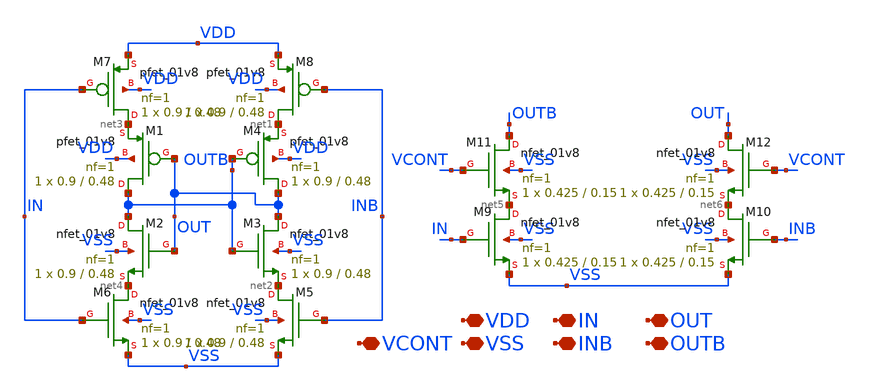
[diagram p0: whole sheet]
** sch_path: xschem/xschem_BGR_Top/Sigma_Delta/VCO/VCO_Delay.sch
**.subckt VCO_Delay VDD VSS IN INB OUT OUTB VCONT
*.iopin VDD
*.iopin VSS
*.iopin IN
*.iopin INB
*.iopin OUT
*.iopin OUTB
*.iopin VCONT
XM4 OUT OUTB net1 VDD sky130_fd_pr__pfet_01v8 L=0.48 W=0.9 nf=1 ad='int((nf+1)/2) * W/nf * 0.29' as='int((nf+2)/2) * W/nf * 0.29'
+ pd='2*int((nf+1)/2) * (W/nf + 0.29)' ps='2*int((nf+2)/2) * (W/nf + 0.29)' nrd='0.29 / W' nrs='0.29 / W'
+ sa=0 sb=0 sd=0 mult=1 m=1
XM3 OUT OUTB net2 VSS sky130_fd_pr__nfet_01v8 L=0.48 W=0.9 nf=1 ad='int((nf+1)/2) * W/nf * 0.29' as='int((nf+2)/2) * W/nf * 0.29'
+ pd='2*int((nf+1)/2) * (W/nf + 0.29)' ps='2*int((nf+2)/2) * (W/nf + 0.29)' nrd='0.29 / W' nrs='0.29 / W'
+ sa=0 sb=0 sd=0 mult=1 m=1
XM1 OUTB OUT net3 VDD sky130_fd_pr__pfet_01v8 L=0.48 W=0.9 nf=1 ad='int((nf+1)/2) * W/nf * 0.29' as='int((nf+2)/2) * W/nf * 0.29'
+ pd='2*int((nf+1)/2) * (W/nf + 0.29)' ps='2*int((nf+2)/2) * (W/nf + 0.29)' nrd='0.29 / W' nrs='0.29 / W'
+ sa=0 sb=0 sd=0 mult=1 m=1
XM2 OUTB OUT net4 VSS sky130_fd_pr__nfet_01v8 L=0.48 W=0.9 nf=1 ad='int((nf+1)/2) * W/nf * 0.29' as='int((nf+2)/2) * W/nf * 0.29'
+ pd='2*int((nf+1)/2) * (W/nf + 0.29)' ps='2*int((nf+2)/2) * (W/nf + 0.29)' nrd='0.29 / W' nrs='0.29 / W'
+ sa=0 sb=0 sd=0 mult=1 m=1
XM5 net2 INB VSS VSS sky130_fd_pr__nfet_01v8 L=0.48 W=0.9 nf=1 ad='int((nf+1)/2) * W/nf * 0.29' as='int((nf+2)/2) * W/nf * 0.29'
+ pd='2*int((nf+1)/2) * (W/nf + 0.29)' ps='2*int((nf+2)/2) * (W/nf + 0.29)' nrd='0.29 / W' nrs='0.29 / W'
+ sa=0 sb=0 sd=0 mult=1 m=1
XM6 net4 IN VSS VSS sky130_fd_pr__nfet_01v8 L=0.48 W=0.9 nf=1 ad='int((nf+1)/2) * W/nf * 0.29' as='int((nf+2)/2) * W/nf * 0.29'
+ pd='2*int((nf+1)/2) * (W/nf + 0.29)' ps='2*int((nf+2)/2) * (W/nf + 0.29)' nrd='0.29 / W' nrs='0.29 / W'
+ sa=0 sb=0 sd=0 mult=1 m=1
XM7 net3 IN VDD VDD sky130_fd_pr__pfet_01v8 L=0.48 W=0.9 nf=1 ad='int((nf+1)/2) * W/nf * 0.29' as='int((nf+2)/2) * W/nf * 0.29'
+ pd='2*int((nf+1)/2) * (W/nf + 0.29)' ps='2*int((nf+2)/2) * (W/nf + 0.29)' nrd='0.29 / W' nrs='0.29 / W'
+ sa=0 sb=0 sd=0 mult=1 m=1
XM8 net1 INB VDD VDD sky130_fd_pr__pfet_01v8 L=0.48 W=0.9 nf=1 ad='int((nf+1)/2) * W/nf * 0.29' as='int((nf+2)/2) * W/nf * 0.29'
+ pd='2*int((nf+1)/2) * (W/nf + 0.29)' ps='2*int((nf+2)/2) * (W/nf + 0.29)' nrd='0.29 / W' nrs='0.29 / W'
+ sa=0 sb=0 sd=0 mult=1 m=1
XM11 OUTB VCONT net5 VSS sky130_fd_pr__nfet_01v8 L=0.15 W=0.425 nf=1 ad='int((nf+1)/2) * W/nf * 0.29'
+ as='int((nf+2)/2) * W/nf * 0.29' pd='2*int((nf+1)/2) * (W/nf + 0.29)' ps='2*int((nf+2)/2) * (W/nf + 0.29)'
+ nrd='0.29 / W' nrs='0.29 / W' sa=0 sb=0 sd=0 mult=1 m=1
XM9 net5 IN VSS VSS sky130_fd_pr__nfet_01v8 L=0.15 W=0.425 nf=1 ad='int((nf+1)/2) * W/nf * 0.29' as='int((nf+2)/2) * W/nf * 0.29'
+ pd='2*int((nf+1)/2) * (W/nf + 0.29)' ps='2*int((nf+2)/2) * (W/nf + 0.29)' nrd='0.29 / W' nrs='0.29 / W'
+ sa=0 sb=0 sd=0 mult=1 m=1
XM10 net6 INB VSS VSS sky130_fd_pr__nfet_01v8 L=0.15 W=0.425 nf=1 ad='int((nf+1)/2) * W/nf * 0.29' as='int((nf+2)/2) * W/nf * 0.29'
+ pd='2*int((nf+1)/2) * (W/nf + 0.29)' ps='2*int((nf+2)/2) * (W/nf + 0.29)' nrd='0.29 / W' nrs='0.29 / W'
+ sa=0 sb=0 sd=0 mult=1 m=1
XM12 OUT VCONT net6 VSS sky130_fd_pr__nfet_01v8 L=0.15 W=0.425 nf=1 ad='int((nf+1)/2) * W/nf * 0.29'
+ as='int((nf+2)/2) * W/nf * 0.29' pd='2*int((nf+1)/2) * (W/nf + 0.29)' ps='2*int((nf+2)/2) * (W/nf + 0.29)'
+ nrd='0.29 / W' nrs='0.29 / W' sa=0 sb=0 sd=0 mult=1 m=1
**.ends
.end
